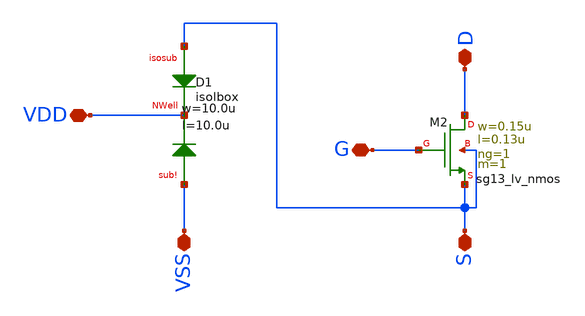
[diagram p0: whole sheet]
** sch_path: ihp-sg13g2/schematic/xschem/sg13_dnwell_nmos.sch
**.subckt sg13_dnwell_nmos VSS S VDD G D
*.iopin VSS
*.iopin S
*.iopin VDD
*.iopin G
*.iopin D
XD1 S VDD VSS isolbox l=10.0u w=10.0u
XM2 D G S S sg13_lv_nmos w=0.15u l=0.13u ng=1 m=1 mm_ok=1
**.ends
.end
